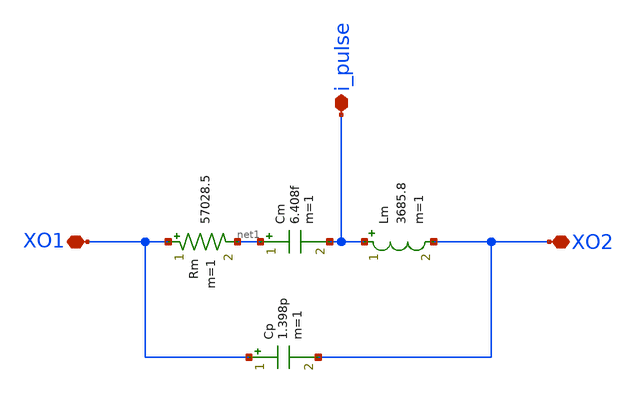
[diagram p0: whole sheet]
** sch_path: xtal_model.sch
**.subckt xtal_model XO2 XO1 i_pulse
*.iopin XO2
*.iopin XO1
*.iopin i_pulse
Rm XO1 net1 57028.5 m=1
Cm net1 i_pulse 6.408f m=1
Cp XO1 XO2 1.398p m=1
Lm i_pulse XO2 3685.8 m=1
**.ends
.end
